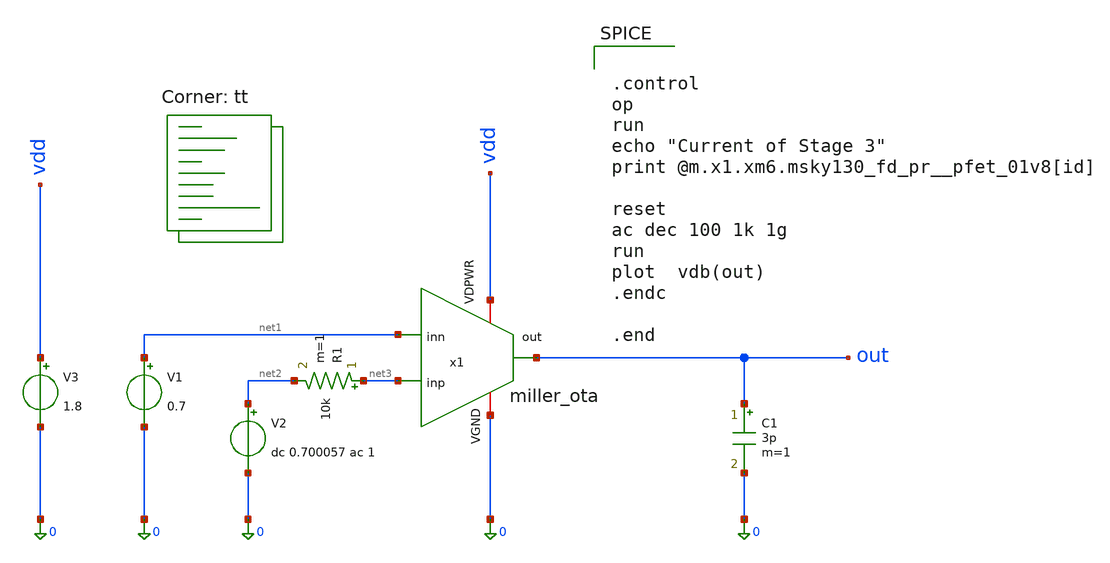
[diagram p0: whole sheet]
** sch_path: src/xschem/miller_ota_test_openLoop.sch
**.subckt miller_ota_test_openLoop
x1 vdd out net1 net3 0 miller_ota
V1 net1 0 0.7
V2 net2 0 dc 0.700057 ac 1
R1 net3 net2 10k m=1
C1 out 0 3p m=1
V3 vdd 0 1.8
**** begin user architecture code


.control
op
run
echo "Current of Stage 3"
print @m.x1.xm6.msky130_fd_pr__pfet_01v8[id]

reset
ac dec 100 1k 1g
run
plot  vdb(out)
.endc

.end

.lib $::SKYWATER_MODELS/sky130.lib.spice tt
**** end user architecture code
**.ends
.end
